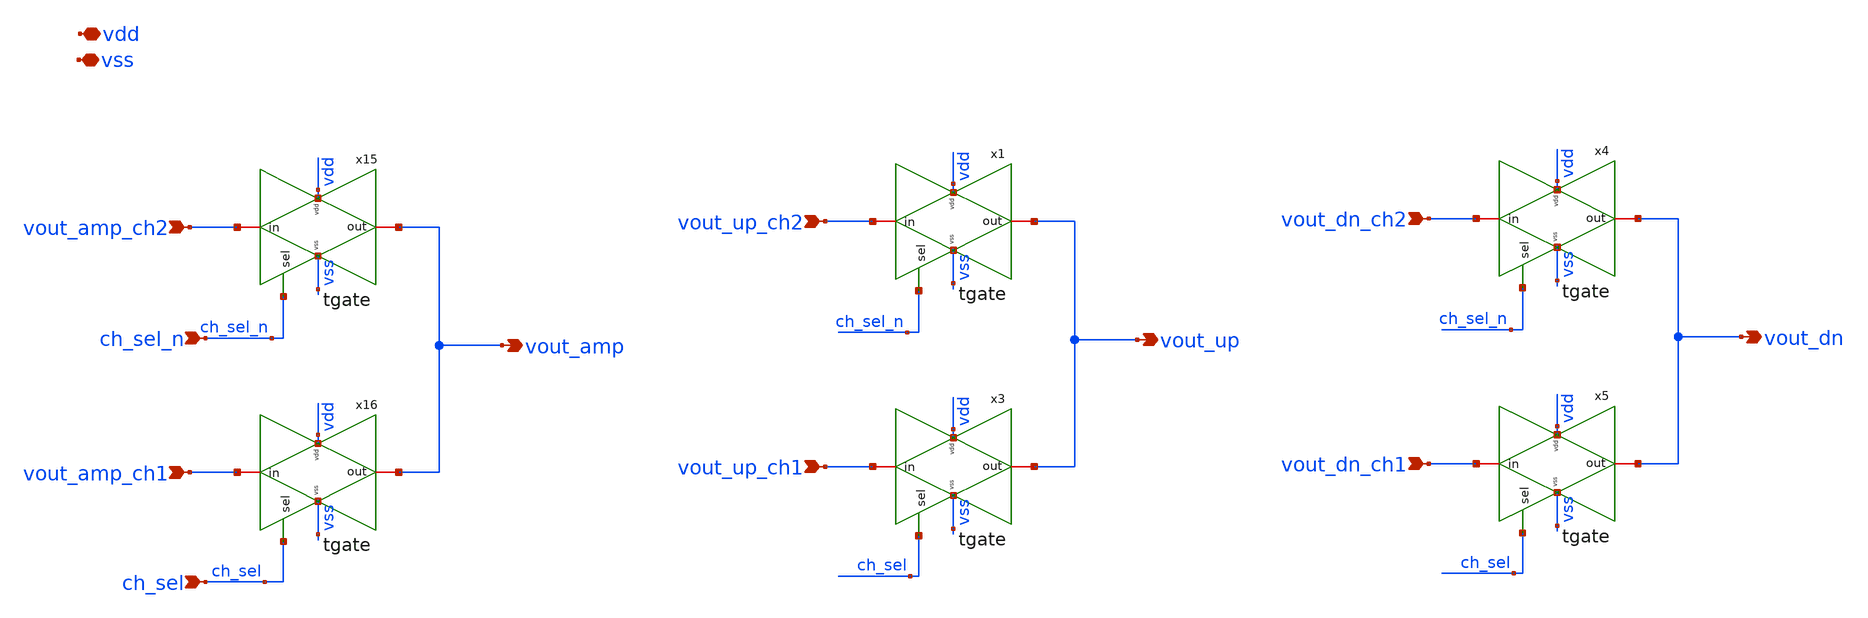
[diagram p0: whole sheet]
** sch_path: v2_feature_extr_withf/output_sel_L.sch
**.subckt output_sel_L vout_amp vout_amp_ch2 vout_amp_ch1 vout_up vout_up_ch2 vout_up_ch1 vout_dn
*+ vout_dn_ch2 vout_dn_ch1 ch_sel_n ch_sel vdd vss
*.opin vout_amp
*.ipin vout_amp_ch2
*.ipin vout_amp_ch1
*.opin vout_up
*.ipin vout_up_ch2
*.ipin vout_up_ch1
*.opin vout_dn
*.ipin vout_dn_ch2
*.ipin vout_dn_ch1
*.ipin ch_sel_n
*.ipin ch_sel
*.iopin vdd
*.iopin vss
x15 vss vdd vout_amp_ch2 vout_amp ch_sel_n tgate
x16 vss vdd vout_amp_ch1 vout_amp ch_sel tgate
x1 vss vdd vout_up_ch2 vout_up ch_sel_n tgate
x3 vss vdd vout_up_ch1 vout_up ch_sel tgate
x4 vss vdd vout_dn_ch2 vout_dn ch_sel_n tgate
x5 vss vdd vout_dn_ch1 vout_dn ch_sel tgate
**.ends
.end
